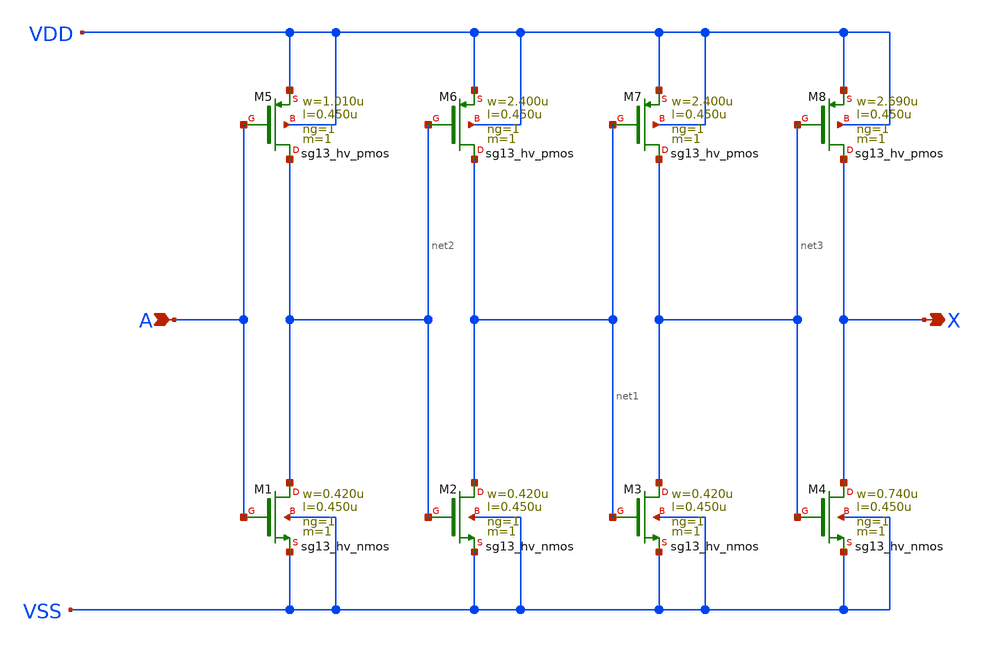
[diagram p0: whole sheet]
** sch_path: ihp-sg13g2/libs.ref/sg13g2_stdcell_hv/sch/xschem/sg13g2_hv_dlygate4sd1_1.sch
* Copyright 2023 IHP PDK Authors
* Licensed under the Apache License, Version 2.0 (the "License");
* you may not use this file except in compliance with the License.
* You may obtain a copy of the License at
* https://www.apache.org/licenses/LICENSE-2.0
* Unless required by applicable law or agreed to in writing, software
* distributed under the License is distributed on an "AS IS" BASIS,
* WITHOUT WARRANTIES OR CONDITIONS OF ANY KIND, either express or implied.
* See the License for the specific language governing permissions and
* limitations under the License.
**.subckt sg13g2_hv_dlygate4sd1_1 A X
*.ipin A
*.opin X
XM1 net2 A VSS VSS sg13_hv_nmos w=0.420u l=0.450u ng=1 m=1 mm_ok=1
XM2 net1 net2 VSS VSS sg13_hv_nmos w=0.420u l=0.450u ng=1 m=1 mm_ok=1
XM3 net3 net1 VSS VSS sg13_hv_nmos w=0.420u l=0.450u ng=1 m=1 mm_ok=1
XM4 X net3 VSS VSS sg13_hv_nmos w=0.740u l=0.450u ng=1 m=1 mm_ok=1
XM5 net2 A VDD VDD sg13_hv_pmos w=1.010u l=0.450u ng=1 m=1 mm_ok=1
XM6 net1 net2 VDD VDD sg13_hv_pmos w=2.400u l=0.450u ng=1 m=1 mm_ok=1
XM7 net3 net1 VDD VDD sg13_hv_pmos w=2.400u l=0.450u ng=1 m=1 mm_ok=1
XM8 X net3 VDD VDD sg13_hv_pmos w=2.690u l=0.450u ng=1 m=1 mm_ok=1
**.ends
.end
